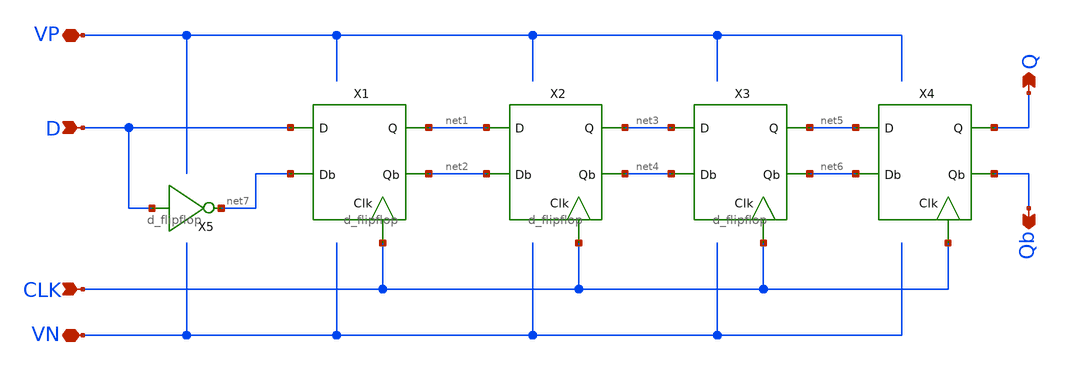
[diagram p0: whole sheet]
** sch_path: simulation/shift_register/andrew_mp2_files/sreg/sreg.sch
**.subckt sreg VP VN CLK D Qb Q
*.iopin VP
*.iopin VN
*.ipin CLK
*.ipin D
*.opin Qb
*.opin Q
X1 D net7 CLK net2 net1 d_flipflop
X2 net1 net2 CLK net4 net3 d_flipflop
X3 net3 net4 CLK net6 net5 d_flipflop
X4 net5 net6 CLK Qb Q d_flipflop
X5 D net7 sreg_inverter
**.ends

* expanding   symbol:  /home/madvlsi/Documents//MADVLSI/mp2/d_flipflop/d_flipflop.sym # of pins=5
** sym_path: simulation/shift_register/andrew_mp2_files/d_flipflop/d_flipflop.sym
** sch_path: simulation/shift_register/andrew_mp2_files/d_flipflop/d_flipflop.sch
.subckt d_flipflop D Db CLK Qb Q
*.ipin D
*.ipin CLK
*.opin Q
*.opin Qb
*.ipin Db
XM1 D CLK net2 VP sky130_fd_pr__pfet_01v8 L=0.15 W=1 nf=1 ad='int((nf+1)/2) * W/nf * 0.29' as='int((nf+2)/2) * W/nf * 0.29'
+ pd='2*int((nf+1)/2) * (W/nf + 0.29)' ps='2*int((nf+2)/2) * (W/nf + 0.29)' nrd='0.29 / W' nrs='0.29 / W'
+ sa=0 sb=0 sd=0 mult=1 m=1
XM2 Db CLK net3 VP sky130_fd_pr__pfet_01v8 L=0.15 W=1 nf=1 ad='int((nf+1)/2) * W/nf * 0.29' as='int((nf+2)/2) * W/nf * 0.29'
+ pd='2*int((nf+1)/2) * (W/nf + 0.29)' ps='2*int((nf+2)/2) * (W/nf + 0.29)' nrd='0.29 / W' nrs='0.29 / W'
+ sa=0 sb=0 sd=0 mult=1 m=1
XM3 VDD net2 net3 VP sky130_fd_pr__pfet_01v8 L=0.15 W=1 nf=1 ad='int((nf+1)/2) * W/nf * 0.29' as='int((nf+2)/2) * W/nf * 0.29'
+ pd='2*int((nf+1)/2) * (W/nf + 0.29)' ps='2*int((nf+2)/2) * (W/nf + 0.29)' nrd='0.29 / W' nrs='0.29 / W'
+ sa=0 sb=0 sd=0 mult=1 m=1
XM5 net3 net2 net1 VN sky130_fd_pr__nfet_01v8 L=0.15 W=1 nf=1 ad='int((nf+1)/2) * W/nf * 0.29' as='int((nf+2)/2) * W/nf * 0.29'
+ pd='2*int((nf+1)/2) * (W/nf + 0.29)' ps='2*int((nf+2)/2) * (W/nf + 0.29)' nrd='0.29 / W' nrs='0.29 / W'
+ sa=0 sb=0 sd=0 mult=1 m=1
XM7 net1 CLK GND VN sky130_fd_pr__nfet_01v8 L=0.15 W=4 nf=1 ad='int((nf+1)/2) * W/nf * 0.29' as='int((nf+2)/2) * W/nf * 0.29'
+ pd='2*int((nf+1)/2) * (W/nf + 0.29)' ps='2*int((nf+2)/2) * (W/nf + 0.29)' nrd='0.29 / W' nrs='0.29 / W'
+ sa=0 sb=0 sd=0 mult=1 m=1
XM8 Q CLK net2 VN sky130_fd_pr__nfet_01v8 L=0.15 W=1 nf=1 ad='int((nf+1)/2) * W/nf * 0.29' as='int((nf+2)/2) * W/nf * 0.29'
+ pd='2*int((nf+1)/2) * (W/nf + 0.29)' ps='2*int((nf+2)/2) * (W/nf + 0.29)' nrd='0.29 / W' nrs='0.29 / W'
+ sa=0 sb=0 sd=0 mult=1 m=1
XM9 Qb CLK net3 VN sky130_fd_pr__nfet_01v8 L=0.15 W=1 nf=1 ad='int((nf+1)/2) * W/nf * 0.29' as='int((nf+2)/2) * W/nf * 0.29'
+ pd='2*int((nf+1)/2) * (W/nf + 0.29)' ps='2*int((nf+2)/2) * (W/nf + 0.29)' nrd='0.29 / W' nrs='0.29 / W'
+ sa=0 sb=0 sd=0 mult=1 m=1
XM10 net4 Q Qb VP sky130_fd_pr__pfet_01v8 L=0.15 W=1 nf=1 ad='int((nf+1)/2) * W/nf * 0.29' as='int((nf+2)/2) * W/nf * 0.29'
+ pd='2*int((nf+1)/2) * (W/nf + 0.29)' ps='2*int((nf+2)/2) * (W/nf + 0.29)' nrd='0.29 / W' nrs='0.29 / W'
+ sa=0 sb=0 sd=0 mult=1 m=1
XM11 net4 Qb Q VP sky130_fd_pr__pfet_01v8 L=0.15 W=1 nf=1 ad='int((nf+1)/2) * W/nf * 0.29' as='int((nf+2)/2) * W/nf * 0.29'
+ pd='2*int((nf+1)/2) * (W/nf + 0.29)' ps='2*int((nf+2)/2) * (W/nf + 0.29)' nrd='0.29 / W' nrs='0.29 / W'
+ sa=0 sb=0 sd=0 mult=1 m=1
XM12 VDD CLK net4 VP sky130_fd_pr__pfet_01v8 L=0.15 W=4 nf=1 ad='int((nf+1)/2) * W/nf * 0.29' as='int((nf+2)/2) * W/nf * 0.29'
+ pd='2*int((nf+1)/2) * (W/nf + 0.29)' ps='2*int((nf+2)/2) * (W/nf + 0.29)' nrd='0.29 / W' nrs='0.29 / W'
+ sa=0 sb=0 sd=0 mult=1 m=1
XM13 Qb Q GND VN sky130_fd_pr__nfet_01v8 L=0.15 W=1 nf=1 ad='int((nf+1)/2) * W/nf * 0.29' as='int((nf+2)/2) * W/nf * 0.29'
+ pd='2*int((nf+1)/2) * (W/nf + 0.29)' ps='2*int((nf+2)/2) * (W/nf + 0.29)' nrd='0.29 / W' nrs='0.29 / W'
+ sa=0 sb=0 sd=0 mult=1 m=1
XM14 Q Qb GND VN sky130_fd_pr__nfet_01v8 L=0.15 W=1 nf=1 ad='int((nf+1)/2) * W/nf * 0.29' as='int((nf+2)/2) * W/nf * 0.29'
+ pd='2*int((nf+1)/2) * (W/nf + 0.29)' ps='2*int((nf+2)/2) * (W/nf + 0.29)' nrd='0.29 / W' nrs='0.29 / W'
+ sa=0 sb=0 sd=0 mult=1 m=1
XM4 VDD net3 net2 VP sky130_fd_pr__pfet_01v8 L=0.15 W=1 nf=1 ad='int((nf+1)/2) * W/nf * 0.29' as='int((nf+2)/2) * W/nf * 0.29'
+ pd='2*int((nf+1)/2) * (W/nf + 0.29)' ps='2*int((nf+2)/2) * (W/nf + 0.29)' nrd='0.29 / W' nrs='0.29 / W'
+ sa=0 sb=0 sd=0 mult=1 m=1
XM6 net2 net3 net1 VN sky130_fd_pr__nfet_01v8 L=0.15 W=1 nf=1 ad='int((nf+1)/2) * W/nf * 0.29' as='int((nf+2)/2) * W/nf * 0.29'
+ pd='2*int((nf+1)/2) * (W/nf + 0.29)' ps='2*int((nf+2)/2) * (W/nf + 0.29)' nrd='0.29 / W' nrs='0.29 / W'
+ sa=0 sb=0 sd=0 mult=1 m=1
.ends


* expanding   symbol:  /home/madvlsi/Documents/MADVLSI/mp2/sreg_inverter/sreg_inverter.sym # of
*+ pins=2
** sym_path: simulation/shift_register/andrew_mp2_files/sreg_inverter/sreg_inverter.sym
** sch_path: simulation/shift_register/andrew_mp2_files/sreg_inverter/sreg_inverter.sch
.subckt sreg_inverter A Y
*.ipin A
*.opin Y
XM1 Y A GND GND sky130_fd_pr__nfet_01v8 L=0.15 W=1 nf=1 ad='int((nf+1)/2) * W/nf * 0.29' as='int((nf+2)/2) * W/nf * 0.29'
+ pd='2*int((nf+1)/2) * (W/nf + 0.29)' ps='2*int((nf+2)/2) * (W/nf + 0.29)' nrd='0.29 / W' nrs='0.29 / W'
+ sa=0 sb=0 sd=0 mult=1 m=1
XM2 Y A VDD VDD sky130_fd_pr__pfet_01v8 L=0.15 W=1 nf=1 ad='int((nf+1)/2) * W/nf * 0.29' as='int((nf+2)/2) * W/nf * 0.29'
+ pd='2*int((nf+1)/2) * (W/nf + 0.29)' ps='2*int((nf+2)/2) * (W/nf + 0.29)' nrd='0.29 / W' nrs='0.29 / W'
+ sa=0 sb=0 sd=0 mult=1 m=1
.ends

.GLOBAL VDD
.GLOBAL GND
.end
